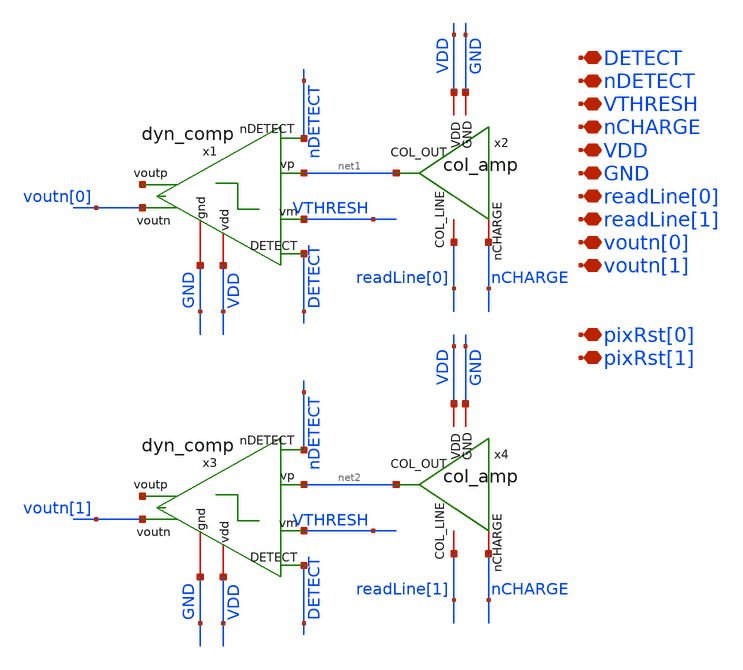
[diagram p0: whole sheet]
** sch_path: analog/xschem/col_amp_2x1.sch
**.subckt col_amp_2x1 nCHARGE VDD GND readLine[0] readLine[1] VTHRESH voutn[0] voutn[1] nDETECT
*+ DETECT pixRst[0] pixRst[1]
*.iopin nCHARGE
*.iopin VDD
*.iopin GND
*.iopin readLine[0]
*.iopin readLine[1]
*.iopin VTHRESH
*.iopin voutn[0]
*.iopin voutn[1]
*.iopin nDETECT
*.iopin DETECT
*.iopin pixRst[0]
*.iopin pixRst[1]
x1 VDD net1 VTHRESH GND nDETECT DETECT net3 voutn[0] dyn_comp
x2 VDD nCHARGE net1 GND readLine[0] col_amp
x3 VDD net2 VTHRESH GND nDETECT DETECT net4 voutn[1] dyn_comp
x4 VDD nCHARGE net2 GND readLine[1] col_amp
**.ends
.end
